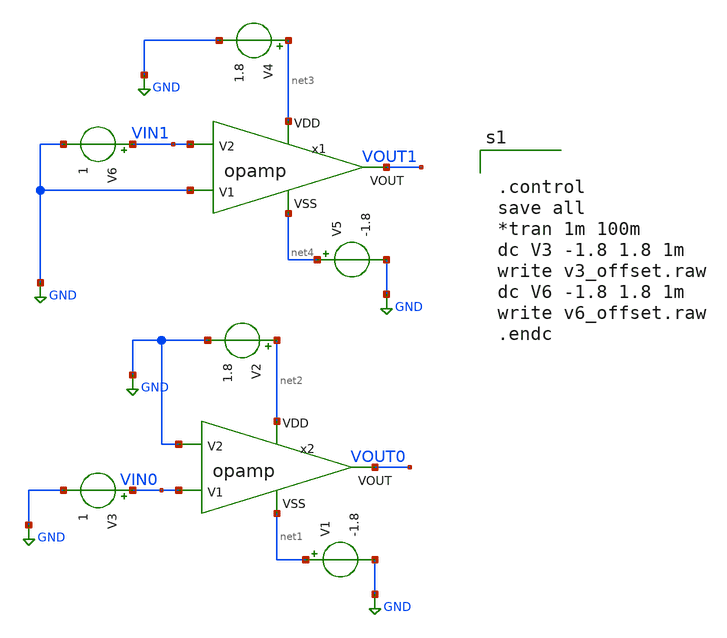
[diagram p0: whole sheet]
** sch_path: xschem/opamp_offset_ss.sch
**.subckt opamp_offset_ss
V2 net2 GND 1.8
V1 net1 GND -1.8
V3 VIN0 GND 1
V5 net4 GND -1.8
V6 VIN1 GND 1
V4 net3 GND 1.8
x1 net3 net4 GND VIN1 VOUT1 opamp
x2 net2 net1 VIN0 GND VOUT0 opamp
**** begin user architecture code


.control
save all
*tran 1m 100m
dc V3 -1.8 1.8 1m
write v3_offset.raw
dc V6 -1.8 1.8 1m
write v6_offset.raw
.endc



** opencircuitdesign pdks install
.lib $::SKYWATER_MODELS/sky130.lib.spice ss


**** end user architecture code
**.ends

* expanding   symbol:  /foss/designs/chipalooza2024/sky130_hcmus_ip__instramp/xschem/opamp.sym # of
*+ pins=5
** sym_path: /foss/designs/chipalooza2024/sky130_hcmus_ip__instramp/xschem/opamp.sym
** sch_path: /foss/designs/chipalooza2024/sky130_hcmus_ip__instramp/xschem/opamp.sch
.subckt opamp VDD VSS V1 V2 VOUT
*.ipin VSS
*.ipin VDD
*.ipin V2
*.ipin V1
*.opin VOUT
XM2 net5 V2 net1 VSS sky130_fd_pr__nfet_g5v0d10v5 L=1 W=18 nf=1 ad='int((nf+1)/2) * W/nf * 0.29' as='int((nf+2)/2) * W/nf * 0.29'
+ pd='2*int((nf+1)/2) * (W/nf + 0.29)' ps='2*int((nf+2)/2) * (W/nf + 0.29)' nrd='0.29 / W' nrs='0.29 / W'
+ sa=0 sb=0 sd=0 mult=1 m=1
XM1 net6 net5 VDD VDD sky130_fd_pr__pfet_g5v0d10v5 L=1 W=30 nf=1 ad='int((nf+1)/2) * W/nf * 0.29' as='int((nf+2)/2) * W/nf * 0.29'
+ pd='2*int((nf+1)/2) * (W/nf + 0.29)' ps='2*int((nf+2)/2) * (W/nf + 0.29)' nrd='0.29 / W' nrs='0.29 / W'
+ sa=0 sb=0 sd=0 mult=1 m=1
XM4 net6 V1 net1 VSS sky130_fd_pr__nfet_g5v0d10v5 L=1 W=18 nf=1 ad='int((nf+1)/2) * W/nf * 0.29' as='int((nf+2)/2) * W/nf * 0.29'
+ pd='2*int((nf+1)/2) * (W/nf + 0.29)' ps='2*int((nf+2)/2) * (W/nf + 0.29)' nrd='0.29 / W' nrs='0.29 / W'
+ sa=0 sb=0 sd=0 mult=1 m=1
XM5 net1 net4 VSS VSS sky130_fd_pr__nfet_g5v0d10v5 L=1 W=15.171 nf=1 ad='int((nf+1)/2) * W/nf * 0.29'
+ as='int((nf+2)/2) * W/nf * 0.29' pd='2*int((nf+1)/2) * (W/nf + 0.29)' ps='2*int((nf+2)/2) * (W/nf + 0.29)'
+ nrd='0.29 / W' nrs='0.29 / W' sa=0 sb=0 sd=0 mult=1 m=1
XM6 VOUT net4 VSS VSS sky130_fd_pr__nfet_g5v0d10v5 L=1 W=19 nf=1 ad='int((nf+1)/2) * W/nf * 0.29' as='int((nf+2)/2) * W/nf * 0.29'
+ pd='2*int((nf+1)/2) * (W/nf + 0.29)' ps='2*int((nf+2)/2) * (W/nf + 0.29)' nrd='0.29 / W' nrs='0.29 / W'
+ sa=0 sb=0 sd=0 mult=1 m=1
XM7 net4 net4 VSS VSS sky130_fd_pr__nfet_g5v0d10v5 L=1 W=20 nf=1 ad='int((nf+1)/2) * W/nf * 0.29' as='int((nf+2)/2) * W/nf * 0.29'
+ pd='2*int((nf+1)/2) * (W/nf + 0.29)' ps='2*int((nf+2)/2) * (W/nf + 0.29)' nrd='0.29 / W' nrs='0.29 / W'
+ sa=0 sb=0 sd=0 mult=1 m=1
XM3 net5 net5 VDD VDD sky130_fd_pr__pfet_g5v0d10v5 L=1 W=30 nf=1 ad='int((nf+1)/2) * W/nf * 0.29' as='int((nf+2)/2) * W/nf * 0.29'
+ pd='2*int((nf+1)/2) * (W/nf + 0.29)' ps='2*int((nf+2)/2) * (W/nf + 0.29)' nrd='0.29 / W' nrs='0.29 / W'
+ sa=0 sb=0 sd=0 mult=1 m=1
XM8 VOUT net6 VDD VDD sky130_fd_pr__pfet_g5v0d10v5 L=1 W=38 nf=1 ad='int((nf+1)/2) * W/nf * 0.29' as='int((nf+2)/2) * W/nf * 0.29'
+ pd='2*int((nf+1)/2) * (W/nf + 0.29)' ps='2*int((nf+2)/2) * (W/nf + 0.29)' nrd='0.29 / W' nrs='0.29 / W'
+ sa=0 sb=0 sd=0 mult=2 m=2
XR3 net2 VDD VSS sky130_fd_pr__res_high_po W=1 L=30 mult=1 m=1
XR1 net3 net2 VSS sky130_fd_pr__res_high_po W=1 L=30 mult=1 m=1
XR2 net4 net3 VSS sky130_fd_pr__res_high_po W=1 L=30 mult=1 m=1
XR4 net7 VOUT VSS sky130_fd_pr__res_high_po W=1 L=5 mult=1 m=1
XC1 net7 net6 sky130_fd_pr__cap_mim_m3_1 W=5.5 L=10 MF=10 m=10
.ends

.GLOBAL GND
.end
